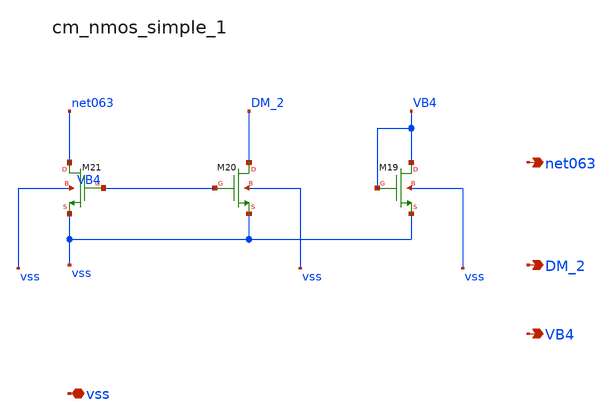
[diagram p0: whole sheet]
** sch_path: analog-db/raw/amp_013_qu2017_azc/hier/blocks/cm_nmos_simple_1.sch
**.subckt cm_nmos_simple_1 vss net063 DM_2 VB4
*.iopin vss
*.opin net063
*.opin DM_2
*.opin VB4
XM19 VB4 VB4 vss vss sg13_lv_nmos w=x_dut_xm19_w l=x_dut_xm19_l ng=1 m=x_dut_xm19_m
XM20 DM_2 VB4 vss vss sg13_lv_nmos w=x_dut_xm20_w l=x_dut_xm20_l ng=1 m=x_dut_xm20_m
XM21 net063 VB4 vss vss sg13_lv_nmos w=x_dut_xm21_w l=x_dut_xm21_l ng=1 m=x_dut_xm21_m
**.ends
.end
